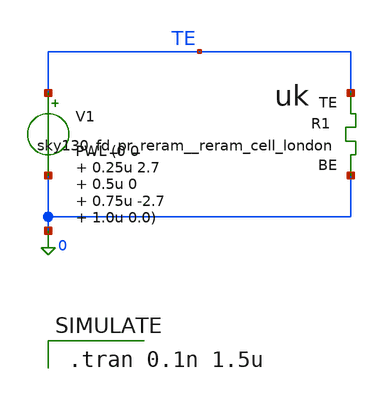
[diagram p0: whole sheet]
** sch_path: memristor_models/rram_london/tb_lissajous.sch
**.subckt tb_lissajous
V1 TE 0 PWL (0 0 0.25u 2.7 0.5u 0 0.75u -2.7 1.0u 0.0)
XR1 TE 0 sky130_fd_pr_reram__reram_cell_london
**** begin user architecture code

.tran 0.1n 1.5u


** opencircuitdesign pdks install
.inc $::SKYWATER_MODELS/sky130_fd_pr_reram__reram_cell_london.spice


.control
save all
run
write tb_lissajous.raw
.endc



**** end user architecture code
**.ends
.end
